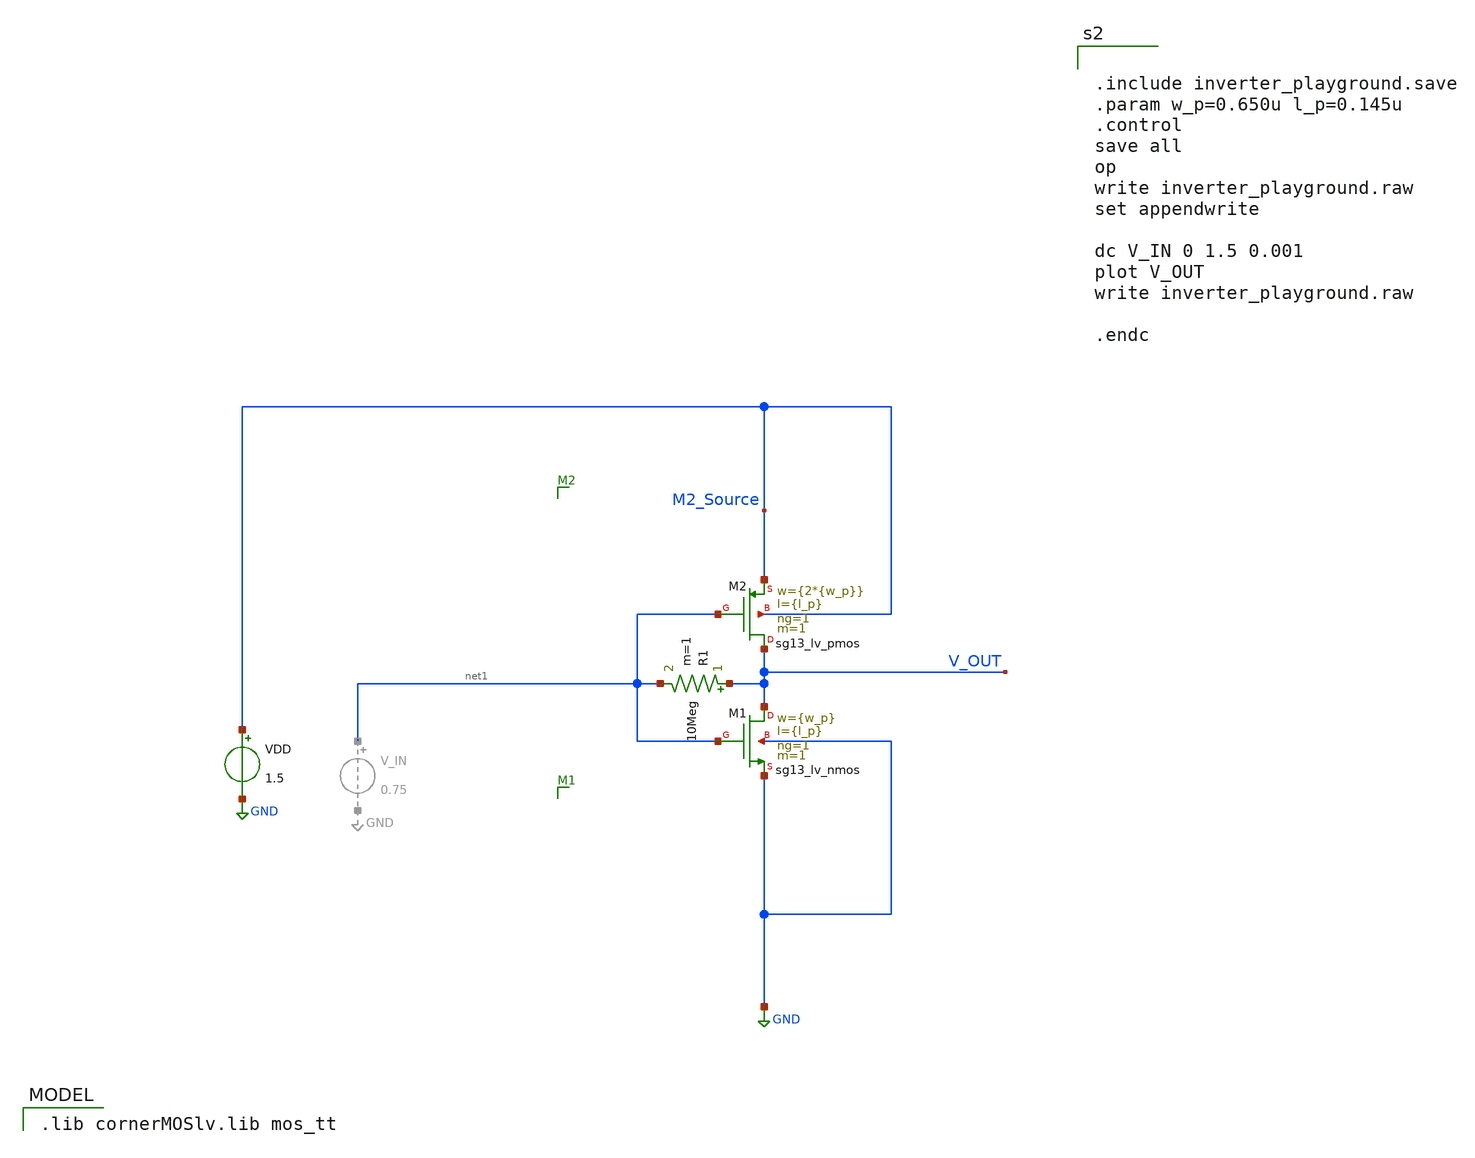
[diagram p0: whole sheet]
** sch_path: inverter_playground.sch
**.subckt inverter_playground
XM1 V_OUT net1 GND GND sg13_lv_nmos w={w_p} l={l_p} ng=1 m=1 mm_ok=1
XM2 V_OUT net1 M2_Source M2_Source sg13_lv_pmos w={2*{w_p}} l={l_p} ng=1 m=1 mm_ok=1
VDD M2_Source GND 1.5
R1 V_OUT net1 10Meg m=1
**** begin user architecture code
 .lib cornerMOSlv.lib mos_tt



.include inverter_playground.save
.param w_p=0.650u l_p=0.145u
.control
save all
op
write inverter_playground.raw
set appendwrite

dc V_IN 0 1.5 0.001
plot V_OUT
write inverter_playground.raw

.endc


**** end user architecture code
**.ends
.GLOBAL GND
.end
